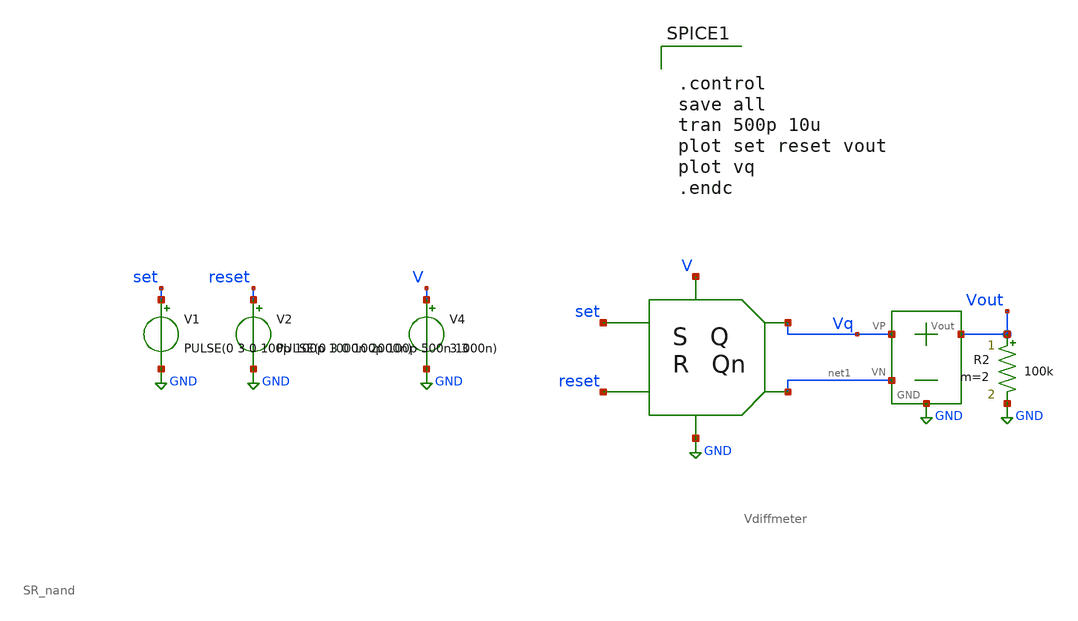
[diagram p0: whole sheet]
** sch_path: SAR_ADC/xschem/test/sr_latch_tb/sin_100k-sin_200k__tb.sch
**.subckt sin_100k-sin_200k__tb
V1 set GND PULSE(0 3 0 100p 100p 1000n 2000n)
V2 reset GND PULSE(0 3 0 100p 100p 500n 1000n)
V4 V GND 3.3
X3 Vq net1 Vout GND Vdiffmeter
R2 Vout GND 100k m=2
X1 set V GND reset Vq net1 SR_nand
**** begin user architecture code


.control
save all
tran 500p 10u
plot set reset vout
plot vq
.endc


.include /foss/pdks/gf180mcuC/libs.tech/ngspice/design.ngspice
.lib /foss/pdks/gf180mcuC/libs.tech/ngspice/sm141064.ngspice typical

**** end user architecture code
**.ends
.GLOBAL GND
.end
